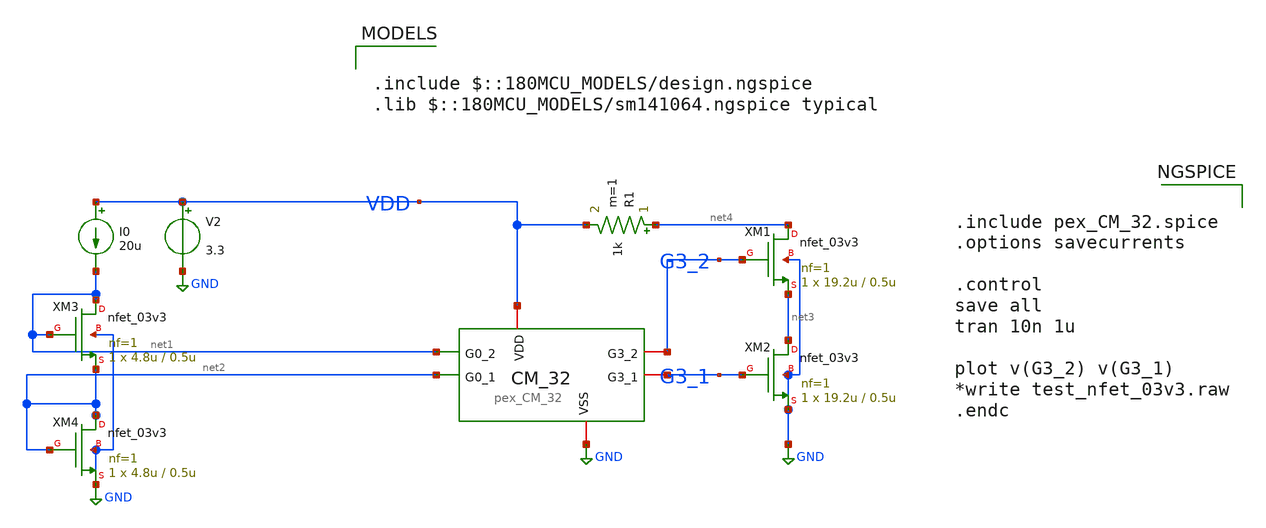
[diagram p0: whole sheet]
** sch_path: DAC_PAKISTAN_01/Pakistan1_Xschem/CM_32_TB.sch
**.subckt CM_32_TB
V2 VDD GND 3.3
x1 G3_1 net1 net2 GND G3_2 VDD pex_CM_32
XM1 net4 G3_2 net3 GND nfet_03v3 L=0.5u W=19.2u nf=1 ad='int((nf+1)/2) * W/nf * 0.18u' as='int((nf+2)/2) * W/nf * 0.18u'
+ pd='2*int((nf+1)/2) * (W/nf + 0.18u)' ps='2*int((nf+2)/2) * (W/nf + 0.18u)' nrd='0.18u / W' nrs='0.18u / W'
+ sa=0 sb=0 sd=0 m=1
XM2 net3 G3_1 GND GND nfet_03v3 L=0.5u W=19.2u nf=1 ad='int((nf+1)/2) * W/nf * 0.18u' as='int((nf+2)/2) * W/nf * 0.18u'
+ pd='2*int((nf+1)/2) * (W/nf + 0.18u)' ps='2*int((nf+2)/2) * (W/nf + 0.18u)' nrd='0.18u / W' nrs='0.18u / W'
+ sa=0 sb=0 sd=0 m=1
R1 net4 VDD 1k m=1
I0 VDD net1 20u
XM3 net1 net1 net2 GND nfet_03v3 L=0.5u W=4.8u nf=1 ad='int((nf+1)/2) * W/nf * 0.18u' as='int((nf+2)/2) * W/nf * 0.18u'
+ pd='2*int((nf+1)/2) * (W/nf + 0.18u)' ps='2*int((nf+2)/2) * (W/nf + 0.18u)' nrd='0.18u / W' nrs='0.18u / W'
+ sa=0 sb=0 sd=0 m=1
XM4 net2 net2 GND GND nfet_03v3 L=0.5u W=4.8u nf=1 ad='int((nf+1)/2) * W/nf * 0.18u' as='int((nf+2)/2) * W/nf * 0.18u'
+ pd='2*int((nf+1)/2) * (W/nf + 0.18u)' ps='2*int((nf+2)/2) * (W/nf + 0.18u)' nrd='0.18u / W' nrs='0.18u / W'
+ sa=0 sb=0 sd=0 m=1
**** begin user architecture code

.include $::180MCU_MODELS/design.ngspice
.lib $::180MCU_MODELS/sm141064.ngspice typical



.include pex_CM_32.spice
.options savecurrents

.control
save all
tran 10n 1u

plot v(G3_2) v(G3_1)
*write test_nfet_03v3.raw
.endc


**** end user architecture code
**.ends
.GLOBAL GND
.end
